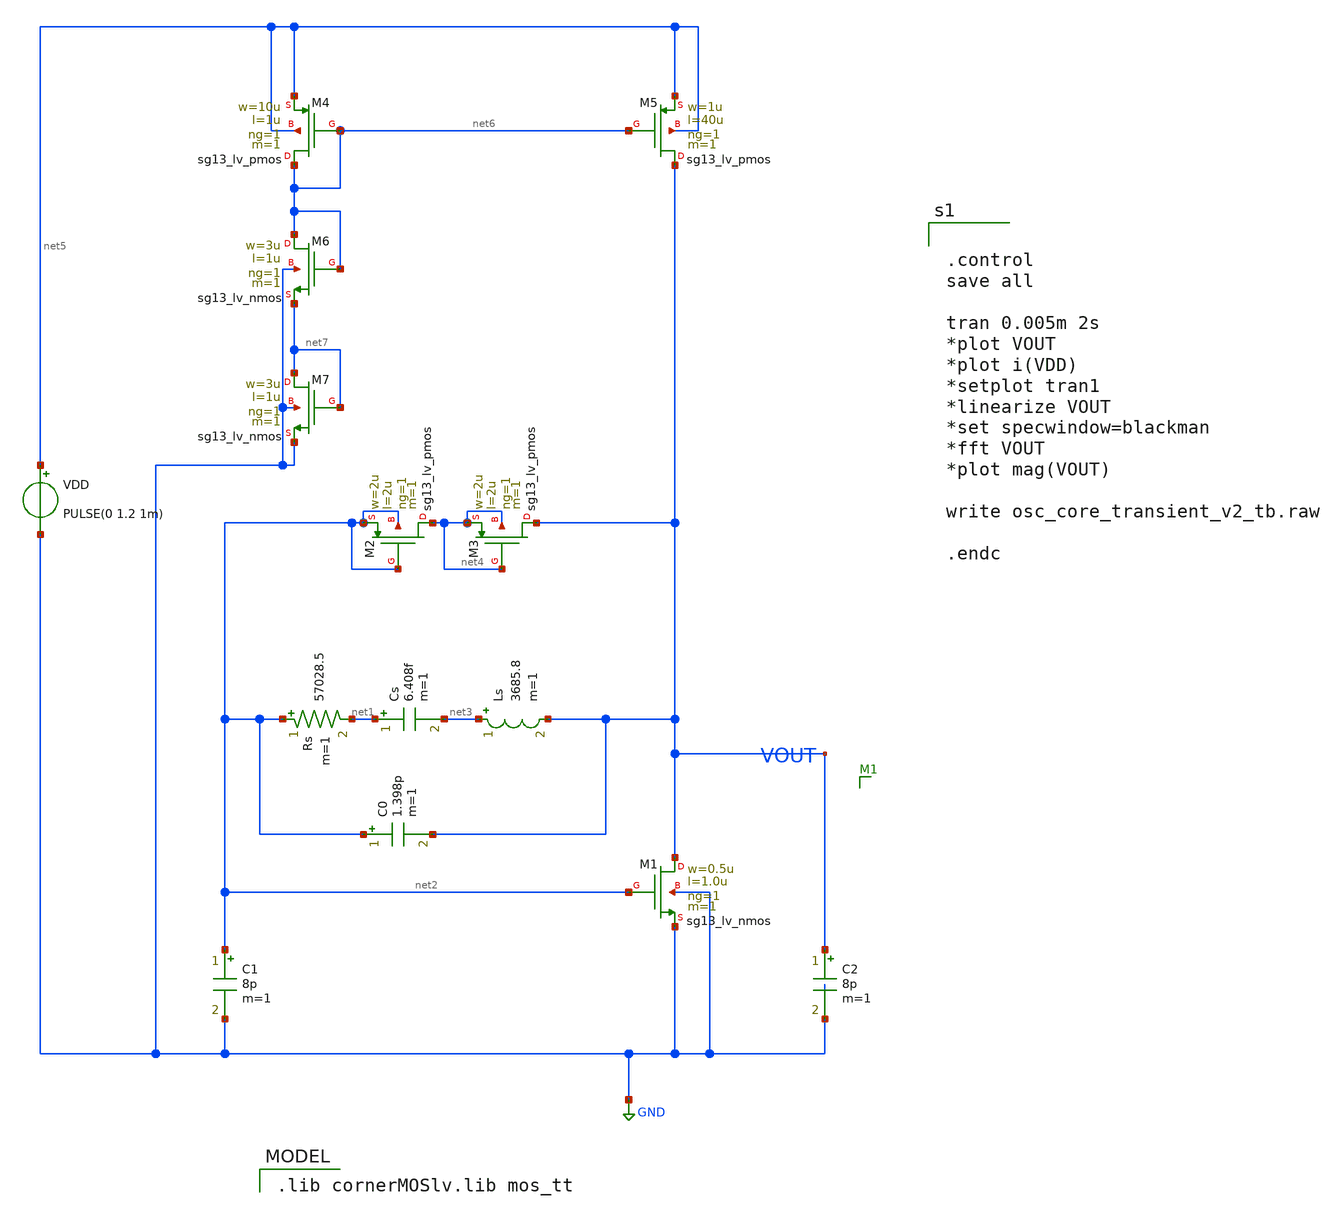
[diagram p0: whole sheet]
** sch_path: osc_core_transient_v2_tb.sch
**.subckt osc_core_transient_v2_tb
XM1 VOUT net2 GND GND sg13_lv_nmos w=0.5u l=1.0u ng=1 m=1 mm_ok=1
C1 net2 GND 8p m=1
C2 VOUT GND 8p m=1
Rs net2 net1 57028.5 m=1
Cs net1 net3 6.408f m=1
C0 net2 VOUT 1.398p m=1
Ls net3 VOUT 3685.8 m=1
VDD net5 GND PULSE(0 1.2 1m)
XM2 net4 net2 net2 net2 sg13_lv_pmos w=2u l=2u ng=1 m=1 mm_ok=1
XM3 VOUT net4 net4 net4 sg13_lv_pmos w=2u l=2u ng=1 m=1 mm_ok=1
XM4 net6 net6 net5 net5 sg13_lv_pmos w=10u l=1u ng=1 m=1 mm_ok=1
XM5 VOUT net6 net5 net5 sg13_lv_pmos w=1u l=40u ng=1 m=1 mm_ok=1
XM6 net6 net6 net7 GND sg13_lv_nmos w=3u l=1u ng=1 m=1 mm_ok=1
XM7 net7 net7 GND GND sg13_lv_nmos w=3u l=1u ng=1 m=1 mm_ok=1
**** begin user architecture code


.control
save all

tran 0.005m 2s
*plot VOUT
*plot i(VDD)
*setplot tran1
*linearize VOUT
*set specwindow=blackman
*fft VOUT
*plot mag(VOUT)

write osc_core_transient_v2_tb.raw

.endc


 .lib cornerMOSlv.lib mos_tt

**** end user architecture code
**.ends
.GLOBAL GND
.end
